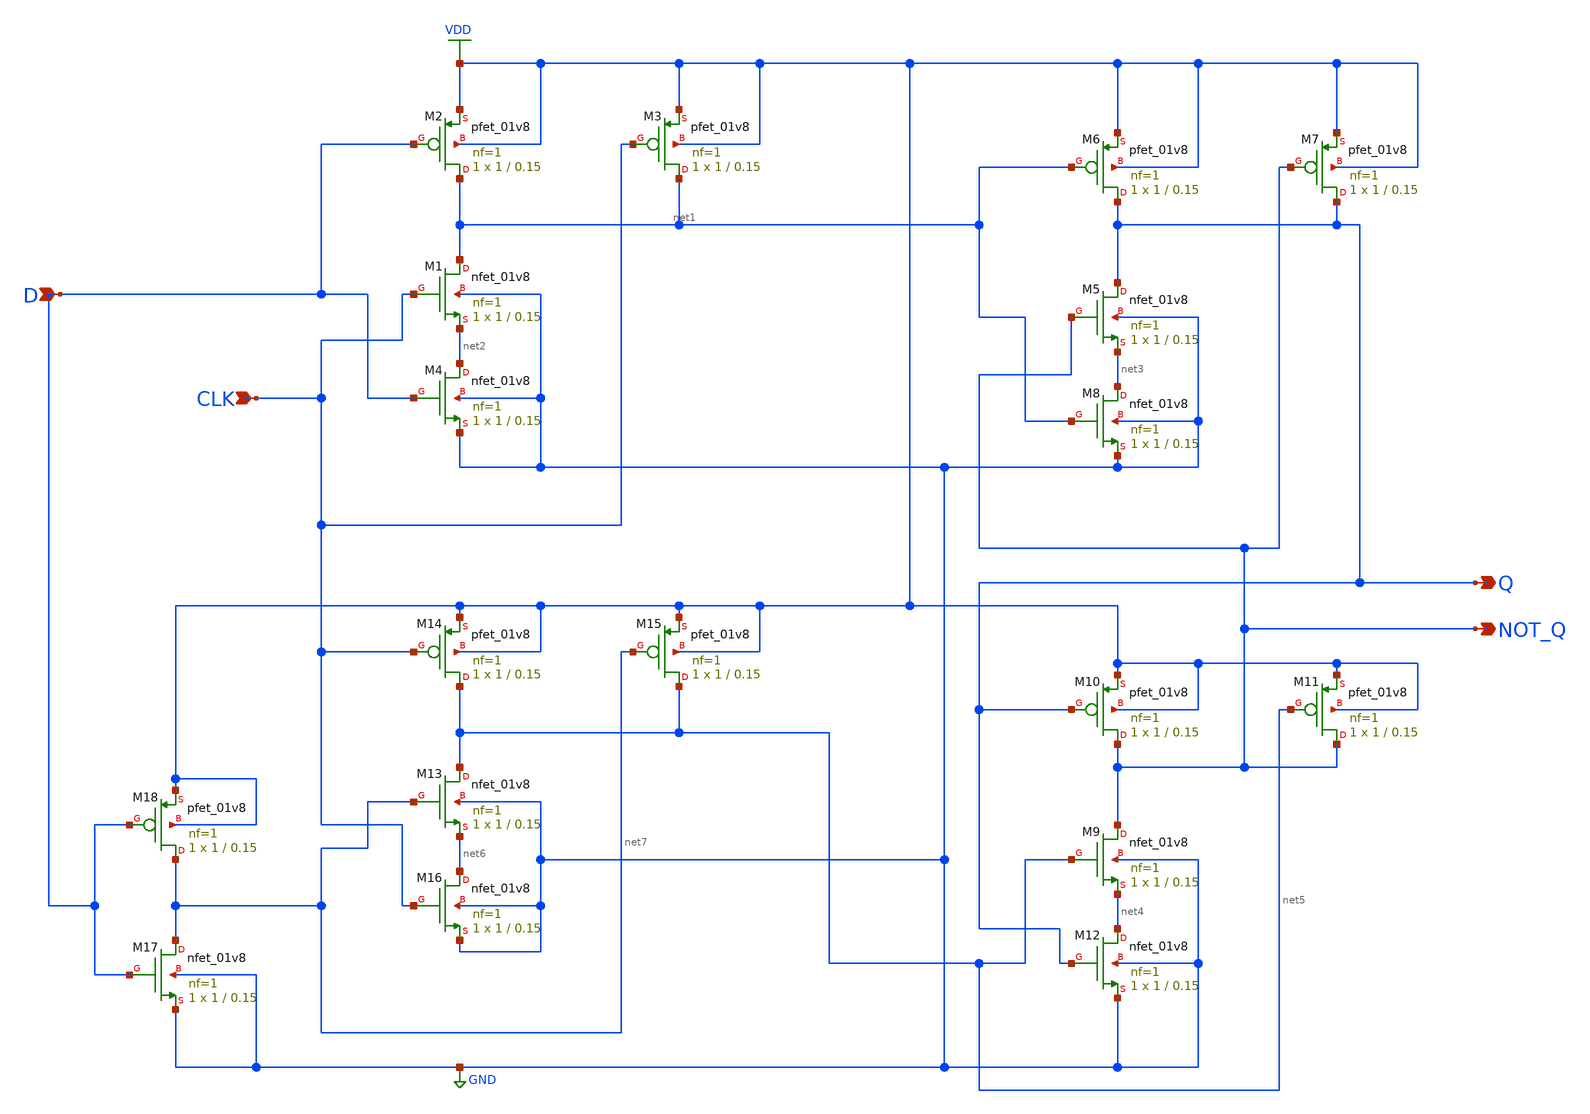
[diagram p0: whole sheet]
** sch_path: library/xschem/Dlatch.sch
**.subckt Dlatch D CLK Q NOT_Q
*.ipin D
*.ipin CLK
*.opin Q
*.opin NOT_Q
XM1 net1 CLK net2 GND sky130_fd_pr__nfet_01v8 L=0.15 W=1 nf=1 ad='int((nf+1)/2) * W/nf * 0.29' as='int((nf+2)/2) * W/nf * 0.29'
+ pd='2*int((nf+1)/2) * (W/nf + 0.29)' ps='2*int((nf+2)/2) * (W/nf + 0.29)' nrd='0.29 / W' nrs='0.29 / W'
+ sa=0 sb=0 sd=0 mult=1 m=1
XM2 net1 D VDD VDD sky130_fd_pr__pfet_01v8 L=0.15 W=1 nf=1 ad='int((nf+1)/2) * W/nf * 0.29' as='int((nf+2)/2) * W/nf * 0.29'
+ pd='2*int((nf+1)/2) * (W/nf + 0.29)' ps='2*int((nf+2)/2) * (W/nf + 0.29)' nrd='0.29 / W' nrs='0.29 / W'
+ sa=0 sb=0 sd=0 mult=1 m=1
XM3 net1 CLK VDD VDD sky130_fd_pr__pfet_01v8 L=0.15 W=1 nf=1 ad='int((nf+1)/2) * W/nf * 0.29' as='int((nf+2)/2) * W/nf * 0.29'
+ pd='2*int((nf+1)/2) * (W/nf + 0.29)' ps='2*int((nf+2)/2) * (W/nf + 0.29)' nrd='0.29 / W' nrs='0.29 / W'
+ sa=0 sb=0 sd=0 mult=1 m=1
XM4 net2 D GND GND sky130_fd_pr__nfet_01v8 L=0.15 W=1 nf=1 ad='int((nf+1)/2) * W/nf * 0.29' as='int((nf+2)/2) * W/nf * 0.29'
+ pd='2*int((nf+1)/2) * (W/nf + 0.29)' ps='2*int((nf+2)/2) * (W/nf + 0.29)' nrd='0.29 / W' nrs='0.29 / W'
+ sa=0 sb=0 sd=0 mult=1 m=1
XM5 Q NOT_Q net3 GND sky130_fd_pr__nfet_01v8 L=0.15 W=1 nf=1 ad='int((nf+1)/2) * W/nf * 0.29' as='int((nf+2)/2) * W/nf * 0.29'
+ pd='2*int((nf+1)/2) * (W/nf + 0.29)' ps='2*int((nf+2)/2) * (W/nf + 0.29)' nrd='0.29 / W' nrs='0.29 / W'
+ sa=0 sb=0 sd=0 mult=1 m=1
XM6 Q net1 VDD VDD sky130_fd_pr__pfet_01v8 L=0.15 W=1 nf=1 ad='int((nf+1)/2) * W/nf * 0.29' as='int((nf+2)/2) * W/nf * 0.29'
+ pd='2*int((nf+1)/2) * (W/nf + 0.29)' ps='2*int((nf+2)/2) * (W/nf + 0.29)' nrd='0.29 / W' nrs='0.29 / W'
+ sa=0 sb=0 sd=0 mult=1 m=1
XM7 Q NOT_Q VDD VDD sky130_fd_pr__pfet_01v8 L=0.15 W=1 nf=1 ad='int((nf+1)/2) * W/nf * 0.29' as='int((nf+2)/2) * W/nf * 0.29'
+ pd='2*int((nf+1)/2) * (W/nf + 0.29)' ps='2*int((nf+2)/2) * (W/nf + 0.29)' nrd='0.29 / W' nrs='0.29 / W'
+ sa=0 sb=0 sd=0 mult=1 m=1
XM8 net3 net1 GND GND sky130_fd_pr__nfet_01v8 L=0.15 W=1 nf=1 ad='int((nf+1)/2) * W/nf * 0.29' as='int((nf+2)/2) * W/nf * 0.29'
+ pd='2*int((nf+1)/2) * (W/nf + 0.29)' ps='2*int((nf+2)/2) * (W/nf + 0.29)' nrd='0.29 / W' nrs='0.29 / W'
+ sa=0 sb=0 sd=0 mult=1 m=1
XM9 NOT_Q net5 net4 GND sky130_fd_pr__nfet_01v8 L=0.15 W=1 nf=1 ad='int((nf+1)/2) * W/nf * 0.29' as='int((nf+2)/2) * W/nf * 0.29'
+ pd='2*int((nf+1)/2) * (W/nf + 0.29)' ps='2*int((nf+2)/2) * (W/nf + 0.29)' nrd='0.29 / W' nrs='0.29 / W'
+ sa=0 sb=0 sd=0 mult=1 m=1
XM10 NOT_Q Q VDD VDD sky130_fd_pr__pfet_01v8 L=0.15 W=1 nf=1 ad='int((nf+1)/2) * W/nf * 0.29' as='int((nf+2)/2) * W/nf * 0.29'
+ pd='2*int((nf+1)/2) * (W/nf + 0.29)' ps='2*int((nf+2)/2) * (W/nf + 0.29)' nrd='0.29 / W' nrs='0.29 / W'
+ sa=0 sb=0 sd=0 mult=1 m=1
XM11 NOT_Q net5 VDD VDD sky130_fd_pr__pfet_01v8 L=0.15 W=1 nf=1 ad='int((nf+1)/2) * W/nf * 0.29' as='int((nf+2)/2) * W/nf * 0.29'
+ pd='2*int((nf+1)/2) * (W/nf + 0.29)' ps='2*int((nf+2)/2) * (W/nf + 0.29)' nrd='0.29 / W' nrs='0.29 / W'
+ sa=0 sb=0 sd=0 mult=1 m=1
XM12 net4 Q GND GND sky130_fd_pr__nfet_01v8 L=0.15 W=1 nf=1 ad='int((nf+1)/2) * W/nf * 0.29' as='int((nf+2)/2) * W/nf * 0.29'
+ pd='2*int((nf+1)/2) * (W/nf + 0.29)' ps='2*int((nf+2)/2) * (W/nf + 0.29)' nrd='0.29 / W' nrs='0.29 / W'
+ sa=0 sb=0 sd=0 mult=1 m=1
XM13 net5 net7 net6 GND sky130_fd_pr__nfet_01v8 L=0.15 W=1 nf=1 ad='int((nf+1)/2) * W/nf * 0.29' as='int((nf+2)/2) * W/nf * 0.29'
+ pd='2*int((nf+1)/2) * (W/nf + 0.29)' ps='2*int((nf+2)/2) * (W/nf + 0.29)' nrd='0.29 / W' nrs='0.29 / W'
+ sa=0 sb=0 sd=0 mult=1 m=1
XM14 net5 CLK VDD VDD sky130_fd_pr__pfet_01v8 L=0.15 W=1 nf=1 ad='int((nf+1)/2) * W/nf * 0.29' as='int((nf+2)/2) * W/nf * 0.29'
+ pd='2*int((nf+1)/2) * (W/nf + 0.29)' ps='2*int((nf+2)/2) * (W/nf + 0.29)' nrd='0.29 / W' nrs='0.29 / W'
+ sa=0 sb=0 sd=0 mult=1 m=1
XM15 net5 net7 VDD VDD sky130_fd_pr__pfet_01v8 L=0.15 W=1 nf=1 ad='int((nf+1)/2) * W/nf * 0.29' as='int((nf+2)/2) * W/nf * 0.29'
+ pd='2*int((nf+1)/2) * (W/nf + 0.29)' ps='2*int((nf+2)/2) * (W/nf + 0.29)' nrd='0.29 / W' nrs='0.29 / W'
+ sa=0 sb=0 sd=0 mult=1 m=1
XM16 net6 CLK GND GND sky130_fd_pr__nfet_01v8 L=0.15 W=1 nf=1 ad='int((nf+1)/2) * W/nf * 0.29' as='int((nf+2)/2) * W/nf * 0.29'
+ pd='2*int((nf+1)/2) * (W/nf + 0.29)' ps='2*int((nf+2)/2) * (W/nf + 0.29)' nrd='0.29 / W' nrs='0.29 / W'
+ sa=0 sb=0 sd=0 mult=1 m=1
XM17 net7 D GND GND sky130_fd_pr__nfet_01v8 L=0.15 W=1 nf=1 ad='int((nf+1)/2) * W/nf * 0.29' as='int((nf+2)/2) * W/nf * 0.29'
+ pd='2*int((nf+1)/2) * (W/nf + 0.29)' ps='2*int((nf+2)/2) * (W/nf + 0.29)' nrd='0.29 / W' nrs='0.29 / W'
+ sa=0 sb=0 sd=0 mult=1 m=1
XM18 net7 D VDD VDD sky130_fd_pr__pfet_01v8 L=0.15 W=1 nf=1 ad='int((nf+1)/2) * W/nf * 0.29' as='int((nf+2)/2) * W/nf * 0.29'
+ pd='2*int((nf+1)/2) * (W/nf + 0.29)' ps='2*int((nf+2)/2) * (W/nf + 0.29)' nrd='0.29 / W' nrs='0.29 / W'
+ sa=0 sb=0 sd=0 mult=1 m=1
**.ends
.GLOBAL VDD
.GLOBAL GND
.end
